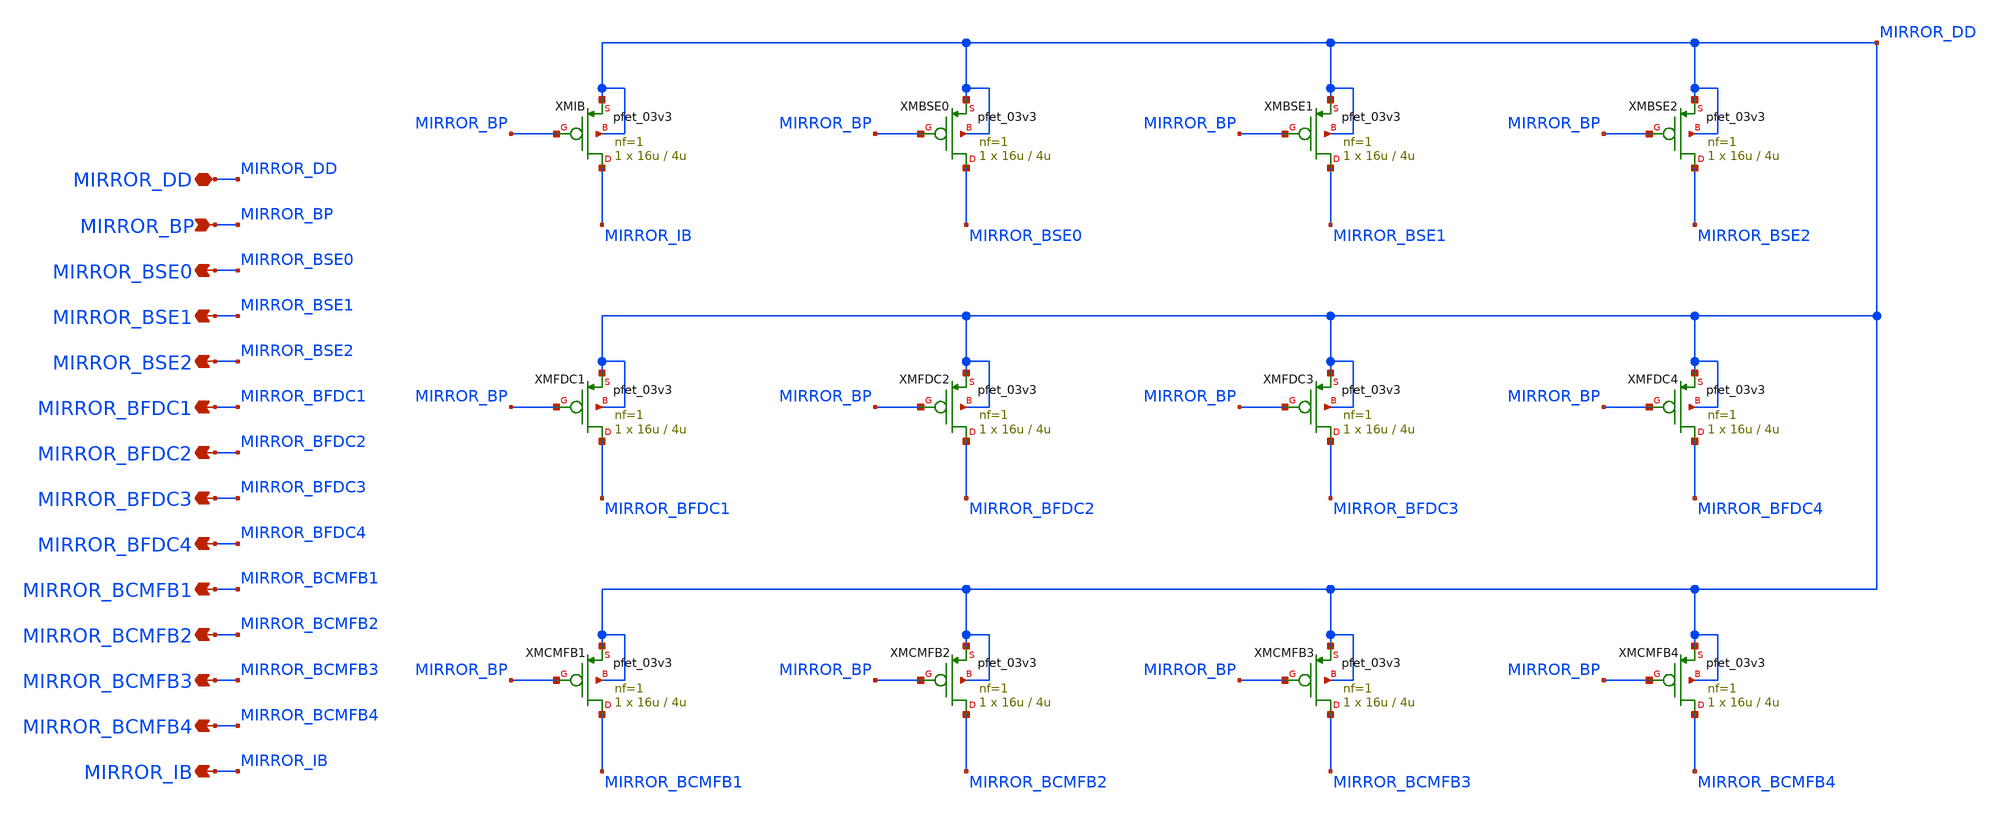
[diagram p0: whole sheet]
** sch_path: Design_Files/IC Design/Schematic/POWER_BLOCKS/MIRROR/MIRROR.sch
**.subckt MIRROR MIRROR_DD MIRROR_BP MIRROR_BSE0 MIRROR_BSE1 MIRROR_BSE2 MIRROR_BFDC1 MIRROR_BFDC2
*+ MIRROR_BFDC3 MIRROR_BFDC4 MIRROR_BCMFB1 MIRROR_BCMFB2 MIRROR_BCMFB3 MIRROR_BCMFB4 MIRROR_IB
*.iopin MIRROR_DD
*.ipin MIRROR_BP
*.opin MIRROR_BSE0
*.opin MIRROR_BSE1
*.opin MIRROR_BSE2
*.opin MIRROR_BFDC1
*.opin MIRROR_BFDC2
*.opin MIRROR_BFDC3
*.opin MIRROR_BFDC4
*.opin MIRROR_BCMFB1
*.opin MIRROR_BCMFB2
*.opin MIRROR_BCMFB3
*.opin MIRROR_BCMFB4
*.opin MIRROR_IB
XMBSE1 MIRROR_BSE1 MIRROR_BP MIRROR_DD MIRROR_DD pfet_03v3 L=4u W=16u nf=1 ad='int((nf+1)/2) * W/nf * 0.18u'
+ as='int((nf+2)/2) * W/nf * 0.18u' pd='2*int((nf+1)/2) * (W/nf + 0.18u)' ps='2*int((nf+2)/2) * (W/nf + 0.18u)'
+ nrd='0.18u / W' nrs='0.18u / W' sa=0 sb=0 sd=0 m=1
XMBSE2 MIRROR_BSE2 MIRROR_BP MIRROR_DD MIRROR_DD pfet_03v3 L=4u W=16u nf=1 ad='int((nf+1)/2) * W/nf * 0.18u'
+ as='int((nf+2)/2) * W/nf * 0.18u' pd='2*int((nf+1)/2) * (W/nf + 0.18u)' ps='2*int((nf+2)/2) * (W/nf + 0.18u)'
+ nrd='0.18u / W' nrs='0.18u / W' sa=0 sb=0 sd=0 m=1
XMFDC1 MIRROR_BFDC1 MIRROR_BP MIRROR_DD MIRROR_DD pfet_03v3 L=4u W=16u nf=1 ad='int((nf+1)/2) * W/nf * 0.18u'
+ as='int((nf+2)/2) * W/nf * 0.18u' pd='2*int((nf+1)/2) * (W/nf + 0.18u)' ps='2*int((nf+2)/2) * (W/nf + 0.18u)'
+ nrd='0.18u / W' nrs='0.18u / W' sa=0 sb=0 sd=0 m=1
XMFDC2 MIRROR_BFDC2 MIRROR_BP MIRROR_DD MIRROR_DD pfet_03v3 L=4u W=16u nf=1 ad='int((nf+1)/2) * W/nf * 0.18u'
+ as='int((nf+2)/2) * W/nf * 0.18u' pd='2*int((nf+1)/2) * (W/nf + 0.18u)' ps='2*int((nf+2)/2) * (W/nf + 0.18u)'
+ nrd='0.18u / W' nrs='0.18u / W' sa=0 sb=0 sd=0 m=1
XMFDC3 MIRROR_BFDC3 MIRROR_BP MIRROR_DD MIRROR_DD pfet_03v3 L=4u W=16u nf=1 ad='int((nf+1)/2) * W/nf * 0.18u'
+ as='int((nf+2)/2) * W/nf * 0.18u' pd='2*int((nf+1)/2) * (W/nf + 0.18u)' ps='2*int((nf+2)/2) * (W/nf + 0.18u)'
+ nrd='0.18u / W' nrs='0.18u / W' sa=0 sb=0 sd=0 m=1
XMFDC4 MIRROR_BFDC4 MIRROR_BP MIRROR_DD MIRROR_DD pfet_03v3 L=4u W=16u nf=1 ad='int((nf+1)/2) * W/nf * 0.18u'
+ as='int((nf+2)/2) * W/nf * 0.18u' pd='2*int((nf+1)/2) * (W/nf + 0.18u)' ps='2*int((nf+2)/2) * (W/nf + 0.18u)'
+ nrd='0.18u / W' nrs='0.18u / W' sa=0 sb=0 sd=0 m=1
XMCMFB1 MIRROR_BCMFB1 MIRROR_BP MIRROR_DD MIRROR_DD pfet_03v3 L=4u W=16u nf=1 ad='int((nf+1)/2) * W/nf * 0.18u'
+ as='int((nf+2)/2) * W/nf * 0.18u' pd='2*int((nf+1)/2) * (W/nf + 0.18u)' ps='2*int((nf+2)/2) * (W/nf + 0.18u)'
+ nrd='0.18u / W' nrs='0.18u / W' sa=0 sb=0 sd=0 m=1
XMCMFB2 MIRROR_BCMFB2 MIRROR_BP MIRROR_DD MIRROR_DD pfet_03v3 L=4u W=16u nf=1 ad='int((nf+1)/2) * W/nf * 0.18u'
+ as='int((nf+2)/2) * W/nf * 0.18u' pd='2*int((nf+1)/2) * (W/nf + 0.18u)' ps='2*int((nf+2)/2) * (W/nf + 0.18u)'
+ nrd='0.18u / W' nrs='0.18u / W' sa=0 sb=0 sd=0 m=1
XMCMFB3 MIRROR_BCMFB3 MIRROR_BP MIRROR_DD MIRROR_DD pfet_03v3 L=4u W=16u nf=1 ad='int((nf+1)/2) * W/nf * 0.18u'
+ as='int((nf+2)/2) * W/nf * 0.18u' pd='2*int((nf+1)/2) * (W/nf + 0.18u)' ps='2*int((nf+2)/2) * (W/nf + 0.18u)'
+ nrd='0.18u / W' nrs='0.18u / W' sa=0 sb=0 sd=0 m=1
XMCMFB4 MIRROR_BCMFB4 MIRROR_BP MIRROR_DD MIRROR_DD pfet_03v3 L=4u W=16u nf=1 ad='int((nf+1)/2) * W/nf * 0.18u'
+ as='int((nf+2)/2) * W/nf * 0.18u' pd='2*int((nf+1)/2) * (W/nf + 0.18u)' ps='2*int((nf+2)/2) * (W/nf + 0.18u)'
+ nrd='0.18u / W' nrs='0.18u / W' sa=0 sb=0 sd=0 m=1
XMBSE0 MIRROR_BSE0 MIRROR_BP MIRROR_DD MIRROR_DD pfet_03v3 L=4u W=16u nf=1 ad='int((nf+1)/2) * W/nf * 0.18u'
+ as='int((nf+2)/2) * W/nf * 0.18u' pd='2*int((nf+1)/2) * (W/nf + 0.18u)' ps='2*int((nf+2)/2) * (W/nf + 0.18u)'
+ nrd='0.18u / W' nrs='0.18u / W' sa=0 sb=0 sd=0 m=1
XMIB MIRROR_IB MIRROR_BP MIRROR_DD MIRROR_DD pfet_03v3 L=4u W=16u nf=1 ad='int((nf+1)/2) * W/nf * 0.18u'
+ as='int((nf+2)/2) * W/nf * 0.18u' pd='2*int((nf+1)/2) * (W/nf + 0.18u)' ps='2*int((nf+2)/2) * (W/nf + 0.18u)'
+ nrd='0.18u / W' nrs='0.18u / W' sa=0 sb=0 sd=0 m=1
**.ends
.end
